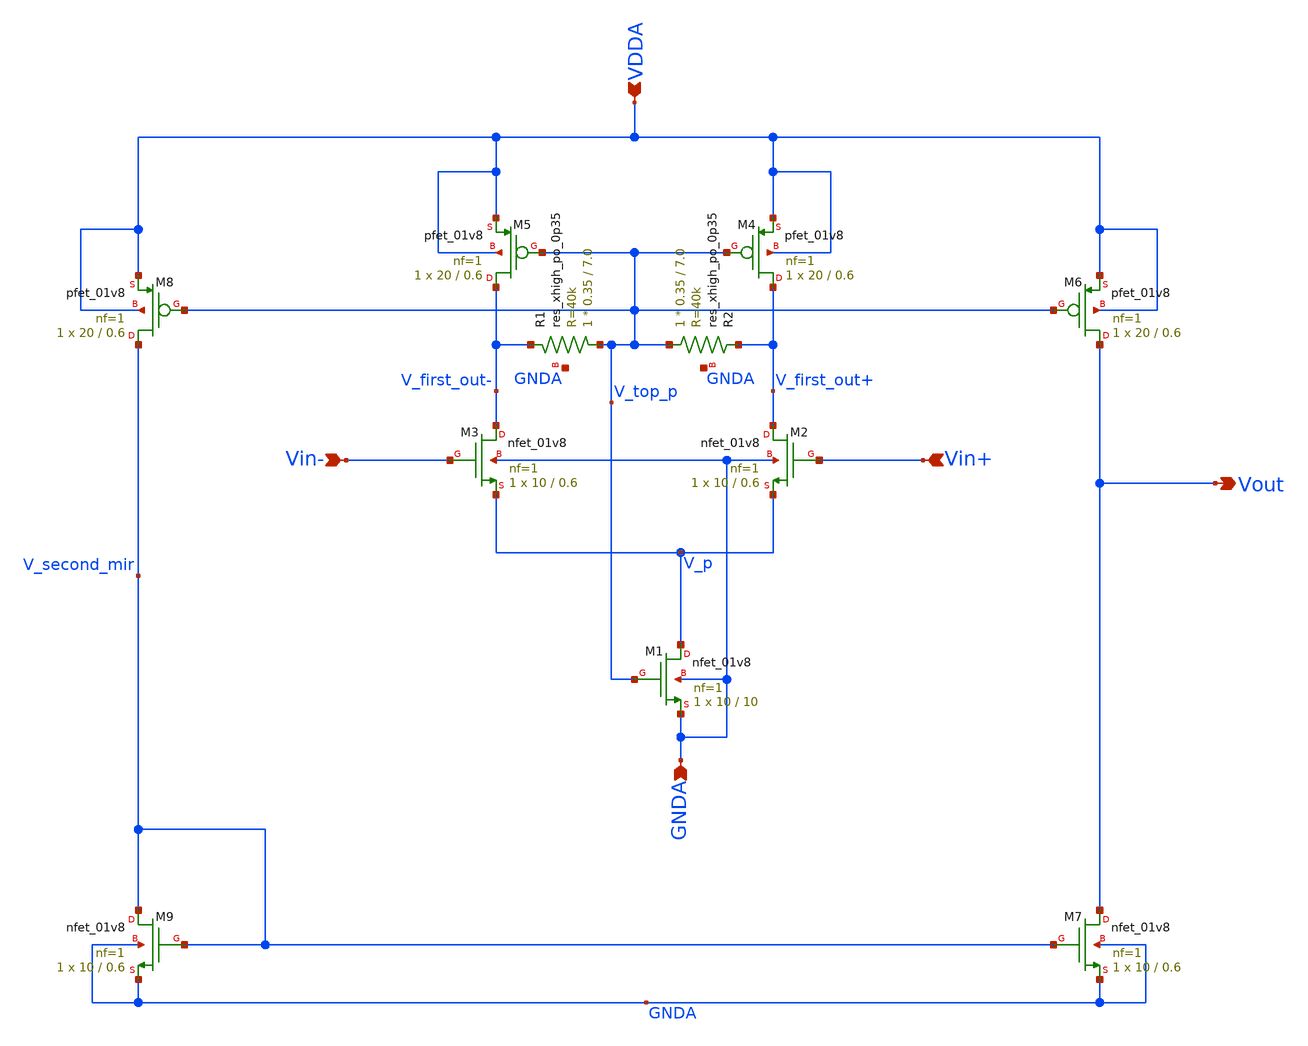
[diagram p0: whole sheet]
** sch_path: projects/bandgapref/xschem_ngspice/new_files/opamp_bandgap_5.sch
**.subckt opamp_bandgap_5 Vin+ Vout Vin- GNDA VDDA
*.ipin Vin+
*.opin Vout
*.ipin Vin-
*.ipin GNDA
*.ipin VDDA
XM4 V_first_out+ V_top_p VDDA VDDA sky130_fd_pr__pfet_01v8 L=0.6 W=20 nf=1 ad='int((nf+1)/2) * W/nf * 0.29'
+ as='int((nf+2)/2) * W/nf * 0.29' pd='2*int((nf+1)/2) * (W/nf + 0.29)' ps='2*int((nf+2)/2) * (W/nf + 0.29)'
+ nrd='0.29 / W' nrs='0.29 / W' sa=0 sb=0 sd=0 mult=1 m=1
XM5 V_first_out- V_top_p VDDA VDDA sky130_fd_pr__pfet_01v8 L=0.6 W=20 nf=1 ad='int((nf+1)/2) * W/nf * 0.29'
+ as='int((nf+2)/2) * W/nf * 0.29' pd='2*int((nf+1)/2) * (W/nf + 0.29)' ps='2*int((nf+2)/2) * (W/nf + 0.29)'
+ nrd='0.29 / W' nrs='0.29 / W' sa=0 sb=0 sd=0 mult=1 m=1
XM2 V_first_out+ Vin+ V_p GNDA sky130_fd_pr__nfet_01v8 L=0.6 W=10 nf=1 ad='int((nf+1)/2) * W/nf * 0.29'
+ as='int((nf+2)/2) * W/nf * 0.29' pd='2*int((nf+1)/2) * (W/nf + 0.29)' ps='2*int((nf+2)/2) * (W/nf + 0.29)'
+ nrd='0.29 / W' nrs='0.29 / W' sa=0 sb=0 sd=0 mult=1 m=1
XM3 V_first_out- Vin- V_p GNDA sky130_fd_pr__nfet_01v8 L=0.6 W=10 nf=1 ad='int((nf+1)/2) * W/nf * 0.29'
+ as='int((nf+2)/2) * W/nf * 0.29' pd='2*int((nf+1)/2) * (W/nf + 0.29)' ps='2*int((nf+2)/2) * (W/nf + 0.29)'
+ nrd='0.29 / W' nrs='0.29 / W' sa=0 sb=0 sd=0 mult=1 m=1
XM1 V_p V_top_p GNDA GNDA sky130_fd_pr__nfet_01v8 L=10 W=10 nf=1 ad='int((nf+1)/2) * W/nf * 0.29' as='int((nf+2)/2) * W/nf * 0.29'
+ pd='2*int((nf+1)/2) * (W/nf + 0.29)' ps='2*int((nf+2)/2) * (W/nf + 0.29)' nrd='0.29 / W' nrs='0.29 / W'
+ sa=0 sb=0 sd=0 mult=1 m=1
XM6 Vout V_top_p VDDA VDDA sky130_fd_pr__pfet_01v8 L=0.6 W=20 nf=1 ad='int((nf+1)/2) * W/nf * 0.29' as='int((nf+2)/2) * W/nf * 0.29'
+ pd='2*int((nf+1)/2) * (W/nf + 0.29)' ps='2*int((nf+2)/2) * (W/nf + 0.29)' nrd='0.29 / W' nrs='0.29 / W'
+ sa=0 sb=0 sd=0 mult=1 m=1
XM7 Vout V_second_mir GNDA GNDA sky130_fd_pr__nfet_01v8 L=0.6 W=10 nf=1 ad='int((nf+1)/2) * W/nf * 0.29'
+ as='int((nf+2)/2) * W/nf * 0.29' pd='2*int((nf+1)/2) * (W/nf + 0.29)' ps='2*int((nf+2)/2) * (W/nf + 0.29)'
+ nrd='0.29 / W' nrs='0.29 / W' sa=0 sb=0 sd=0 mult=1 m=1
XR1 V_top_p V_first_out- GNDA sky130_fd_pr__res_xhigh_po_0p35 L=7.0 mult=1 m=1
XR2 V_top_p V_first_out+ GNDA sky130_fd_pr__res_xhigh_po_0p35 L=7.0 mult=1 m=1
XM8 V_second_mir V_top_p VDDA VDDA sky130_fd_pr__pfet_01v8 L=0.6 W=20 nf=1 ad='int((nf+1)/2) * W/nf * 0.29'
+ as='int((nf+2)/2) * W/nf * 0.29' pd='2*int((nf+1)/2) * (W/nf + 0.29)' ps='2*int((nf+2)/2) * (W/nf + 0.29)'
+ nrd='0.29 / W' nrs='0.29 / W' sa=0 sb=0 sd=0 mult=1 m=1
XM9 V_second_mir V_second_mir GNDA GNDA sky130_fd_pr__nfet_01v8 L=0.6 W=10 nf=1 ad='int((nf+1)/2) * W/nf * 0.29'
+ as='int((nf+2)/2) * W/nf * 0.29' pd='2*int((nf+1)/2) * (W/nf + 0.29)' ps='2*int((nf+2)/2) * (W/nf + 0.29)'
+ nrd='0.29 / W' nrs='0.29 / W' sa=0 sb=0 sd=0 mult=1 m=1
**.ends
.end
